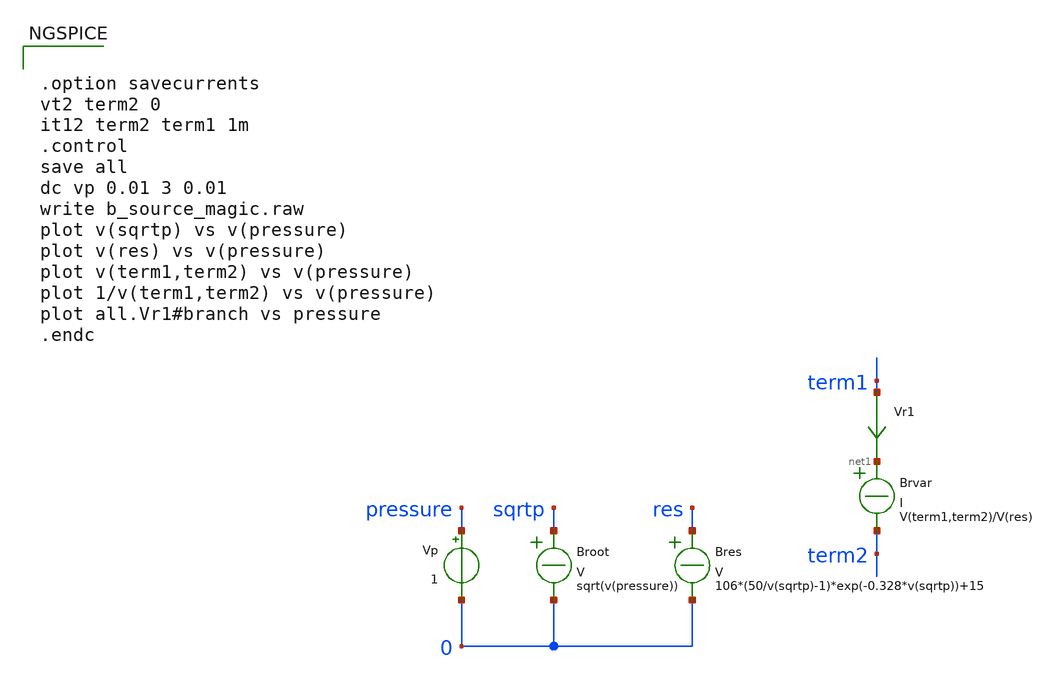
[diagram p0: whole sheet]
** sch_path: sensormodels/piezoresistor.sch
* Copyright 2020 Stefan Frederik Schippers
* Licensed under the Apache License, Version 2.0 (the "License");
* you may not use this file except in compliance with the License.
* You may obtain a copy of the License at
* https://www.apache.org/licenses/LICENSE-2.0
* Unless required by applicable law or agreed to in writing, software
* distributed under the License is distributed on an "AS IS" BASIS,
* WITHOUT WARRANTIES OR CONDITIONS OF ANY KIND, either express or implied.
* See the License for the specific language governing permissions and
* limitations under the License.
**.subckt piezoresistor
Broot sqrtp 0 V = sqrt(v(pressure))
Bres res 0 V = 106*(50/v(sqrtp)-1)*exp(-0.328*v(sqrtp))+15
Brvar net1 term2 I = V(term1,term2)/V(res)
Vp pressure 0 1
Vr1 term1 net1 0
.save i(vr1)
**** begin user architecture code


.option savecurrents
vt2 term2 0
it12 term2 term1 1m
.control
save all
dc vp 0.01 3 0.01
write b_source_magic.raw
plot v(sqrtp) vs v(pressure)
plot v(res) vs v(pressure)
plot v(term1,term2) vs v(pressure)
plot 1/v(term1,term2) vs v(pressure)
plot all.Vr1#branch vs pressure
.endc


**** end user architecture code
**.ends
.end
